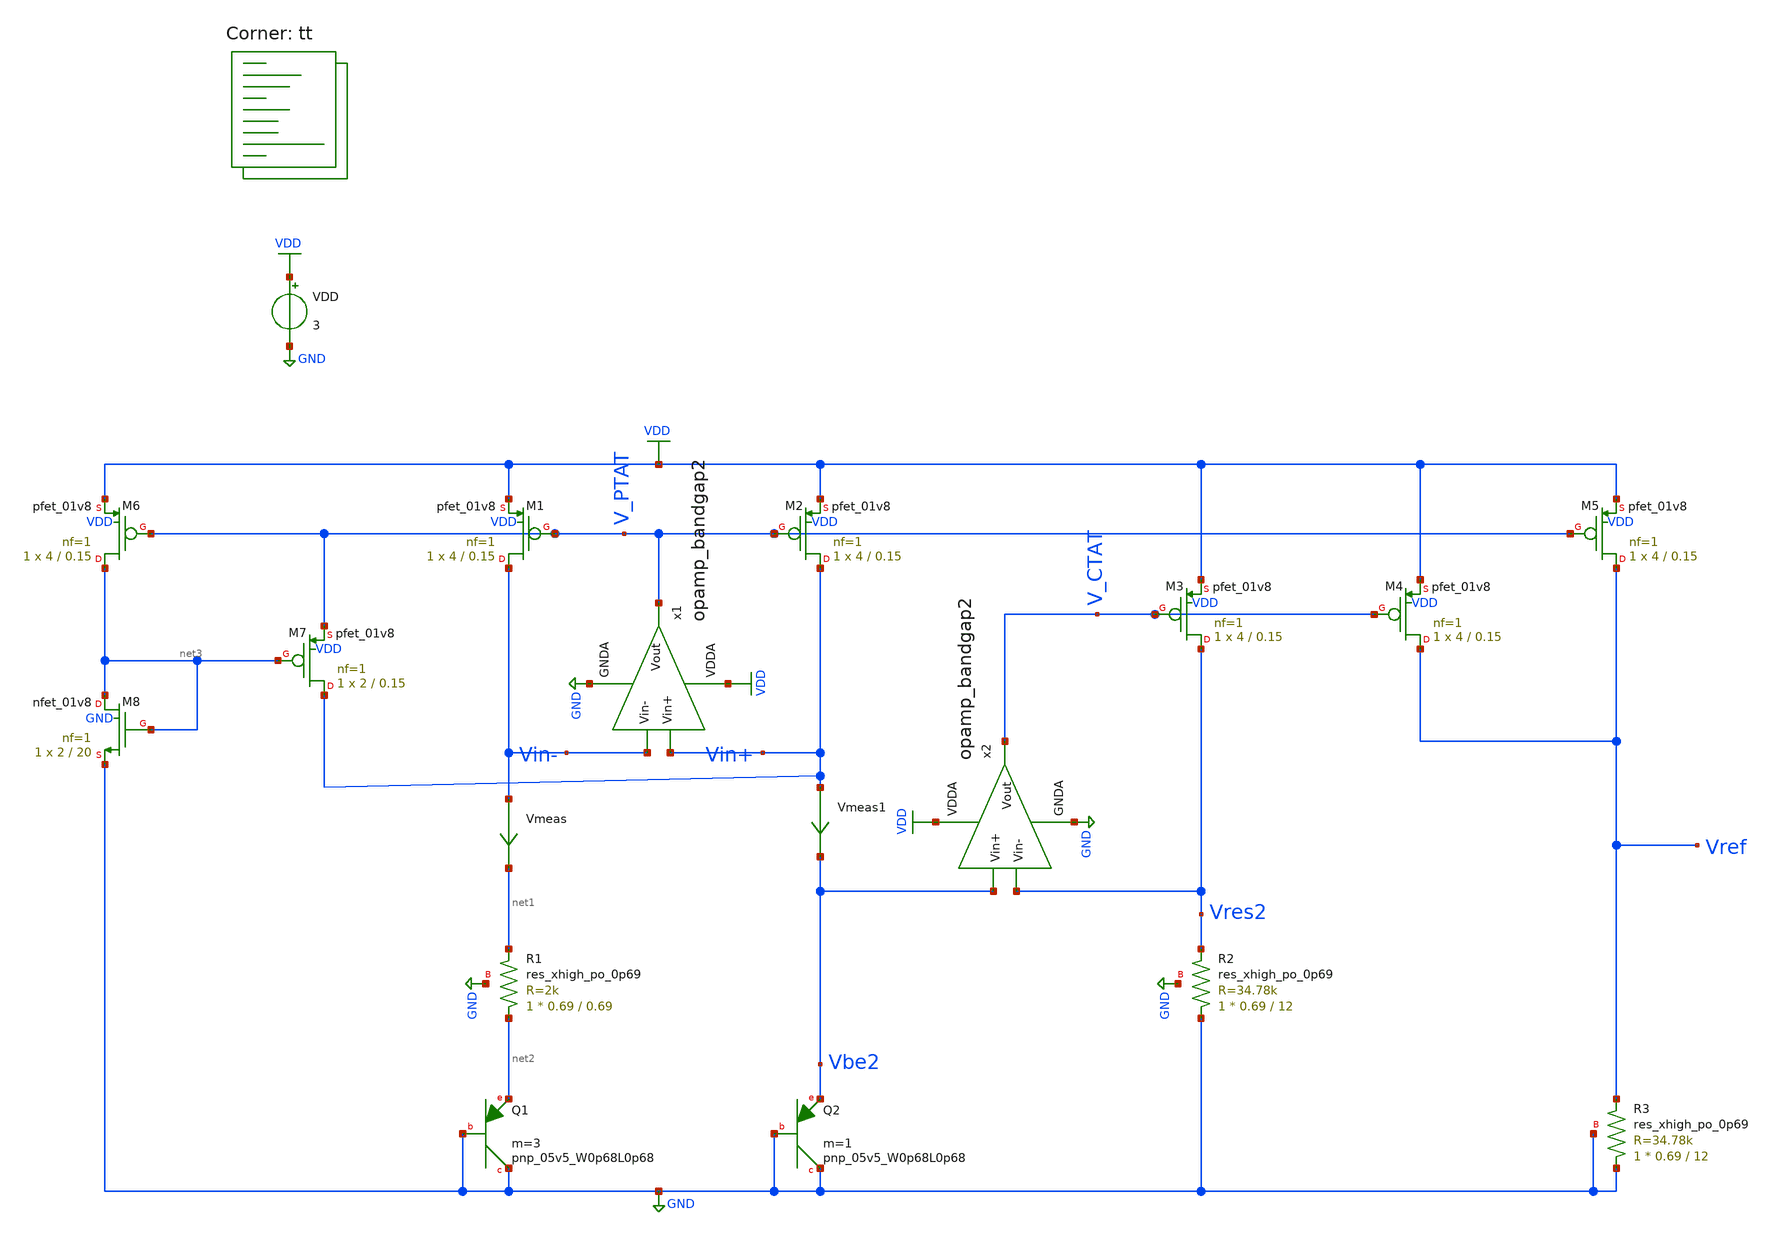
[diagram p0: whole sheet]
** sch_path: projects/bandgapref/xschem_ngspice/old_files/mos_bandgap_baker6.sch
**.subckt mos_bandgap_baker6
VDD VDD GND 3
Vmeas Vin- net1 0
.save i(vmeas)
Vmeas1 Vin+ Vbe2 0
.save i(vmeas1)
x1 VDD V_PTAT Vin- Vin+ GND opamp_bandgap2
XQ1 GND GND net2 sky130_fd_pr__pnp_05v5_W0p68L0p68 m=3
XQ2 GND GND Vbe2 sky130_fd_pr__pnp_05v5_W0p68L0p68 m=1
XR1 net2 net1 GND sky130_fd_pr__res_xhigh_po_0p69 L=0.69 mult=1 m=1
XM1 Vin- V_PTAT VDD VDD sky130_fd_pr__pfet_01v8 L=0.15 W=4 nf=1 ad='int((nf+1)/2) * W/nf * 0.29' as='int((nf+2)/2) * W/nf * 0.29'
+ pd='2*int((nf+1)/2) * (W/nf + 0.29)' ps='2*int((nf+2)/2) * (W/nf + 0.29)' nrd='0.29 / W' nrs='0.29 / W'
+ sa=0 sb=0 sd=0 mult=1 m=1
XM2 Vin+ V_PTAT VDD VDD sky130_fd_pr__pfet_01v8 L=0.15 W=4 nf=1 ad='int((nf+1)/2) * W/nf * 0.29' as='int((nf+2)/2) * W/nf * 0.29'
+ pd='2*int((nf+1)/2) * (W/nf + 0.29)' ps='2*int((nf+2)/2) * (W/nf + 0.29)' nrd='0.29 / W' nrs='0.29 / W'
+ sa=0 sb=0 sd=0 mult=1 m=1
x2 VDD V_CTAT Vres2 Vbe2 GND opamp_bandgap2
XR2 GND Vres2 GND sky130_fd_pr__res_xhigh_po_0p69 L=12 mult=1 m=1
XM3 Vres2 V_CTAT VDD VDD sky130_fd_pr__pfet_01v8 L=0.15 W=4 nf=1 ad='int((nf+1)/2) * W/nf * 0.29' as='int((nf+2)/2) * W/nf * 0.29'
+ pd='2*int((nf+1)/2) * (W/nf + 0.29)' ps='2*int((nf+2)/2) * (W/nf + 0.29)' nrd='0.29 / W' nrs='0.29 / W'
+ sa=0 sb=0 sd=0 mult=1 m=1
XM4 Vref V_CTAT VDD VDD sky130_fd_pr__pfet_01v8 L=0.15 W=4 nf=1 ad='int((nf+1)/2) * W/nf * 0.29' as='int((nf+2)/2) * W/nf * 0.29'
+ pd='2*int((nf+1)/2) * (W/nf + 0.29)' ps='2*int((nf+2)/2) * (W/nf + 0.29)' nrd='0.29 / W' nrs='0.29 / W'
+ sa=0 sb=0 sd=0 mult=1 m=1
XM5 Vref V_PTAT VDD VDD sky130_fd_pr__pfet_01v8 L=0.15 W=4 nf=1 ad='int((nf+1)/2) * W/nf * 0.29' as='int((nf+2)/2) * W/nf * 0.29'
+ pd='2*int((nf+1)/2) * (W/nf + 0.29)' ps='2*int((nf+2)/2) * (W/nf + 0.29)' nrd='0.29 / W' nrs='0.29 / W'
+ sa=0 sb=0 sd=0 mult=1 m=1
XR3 GND Vref GND sky130_fd_pr__res_xhigh_po_0p69 L=12 mult=1 m=1
XM6 net3 V_PTAT VDD VDD sky130_fd_pr__pfet_01v8 L=0.15 W=4 nf=1 ad='int((nf+1)/2) * W/nf * 0.29' as='int((nf+2)/2) * W/nf * 0.29'
+ pd='2*int((nf+1)/2) * (W/nf + 0.29)' ps='2*int((nf+2)/2) * (W/nf + 0.29)' nrd='0.29 / W' nrs='0.29 / W'
+ sa=0 sb=0 sd=0 mult=1 m=1
XM7 Vin+ net3 V_PTAT VDD sky130_fd_pr__pfet_01v8 L=0.15 W=2 nf=1 ad='int((nf+1)/2) * W/nf * 0.29' as='int((nf+2)/2) * W/nf * 0.29'
+ pd='2*int((nf+1)/2) * (W/nf + 0.29)' ps='2*int((nf+2)/2) * (W/nf + 0.29)' nrd='0.29 / W' nrs='0.29 / W'
+ sa=0 sb=0 sd=0 mult=1 m=1
XM8 net3 net3 GND GND sky130_fd_pr__nfet_01v8 L=20 W=2 nf=1 ad='int((nf+1)/2) * W/nf * 0.29' as='int((nf+2)/2) * W/nf * 0.29'
+ pd='2*int((nf+1)/2) * (W/nf + 0.29)' ps='2*int((nf+2)/2) * (W/nf + 0.29)' nrd='0.29 / W' nrs='0.29 / W'
+ sa=0 sb=0 sd=0 mult=1 m=1
**** begin user architecture code
.lib $::SKYWATER_MODELS/sky130.lib.spice tt



.option method=gear
.option wnflag=1
.option savecurrents

.save @m.xm1.msky130_fd_pr__pfet_01v8[gm] @m.xm2.msky130_fd_pr__pfet_01v8[gm] @m.xm3.msky130_fd_pr__pfet_01v8[gm] @m.xm4.msky130_fd_pr__pfet_01v8[gm] @m.xm5.msky130_fd_pr__pfet_01v8[gm] @m.xm6.msky130_fd_pr__pfet_01v8[gm] @m.xm7.msky130_fd_pr__pfet_01v8[gm] @m.xm8.msky130_fd_pr__nfet_01v8[gm]

.control
  save all
  op
  dc VDD 0 3.3 0.1 temp -40 120 1
  * tran 4ns 40us
  remzerovec
  write mos_bandgap_baker6.raw
  set appendwrite
.endc




**** end user architecture code
**.ends

* expanding   symbol:
*+  /foss/designs/my_design/projects/pll/bandgapref/xschem_ngspice/opamp_bandgap2.sym # of pins=5
** sym_path: projects/bandgapref/xschem_ngspice/old_files/opamp_bandgap2.sym
** sch_path: projects/bandgapref/xschem_ngspice/old_files/opamp_bandgap2.sch
.subckt opamp_bandgap2 VDDA Vout Vin- Vin+ GNDA
*.ipin Vin+
*.opin Vout
*.ipin Vin-
*.ipin GNDA
*.ipin VDDA
XM2 net2 Vin- net1 GNDA sky130_fd_pr__nfet_01v8 L=0.6 W=2 nf=2 ad='int((nf+1)/2) * W/nf * 0.29' as='int((nf+2)/2) * W/nf * 0.29'
+ pd='2*int((nf+1)/2) * (W/nf + 0.29)' ps='2*int((nf+2)/2) * (W/nf + 0.29)' nrd='0.29 / W' nrs='0.29 / W'
+ sa=0 sb=0 sd=0 mult=1 m=1
XM3 Vout Vin+ net1 GNDA sky130_fd_pr__nfet_01v8 L=0.6 W=2 nf=2 ad='int((nf+1)/2) * W/nf * 0.29' as='int((nf+2)/2) * W/nf * 0.29'
+ pd='2*int((nf+1)/2) * (W/nf + 0.29)' ps='2*int((nf+2)/2) * (W/nf + 0.29)' nrd='0.29 / W' nrs='0.29 / W'
+ sa=0 sb=0 sd=0 mult=1 m=1
XM1 net1 net1 GNDA GNDA sky130_fd_pr__nfet_01v8 L=0.6 W=4 nf=1 ad='int((nf+1)/2) * W/nf * 0.29' as='int((nf+2)/2) * W/nf * 0.29'
+ pd='2*int((nf+1)/2) * (W/nf + 0.29)' ps='2*int((nf+2)/2) * (W/nf + 0.29)' nrd='0.29 / W' nrs='0.29 / W'
+ sa=0 sb=0 sd=0 mult=1 m=1
XM4 Vout net2 VDDA VDDA sky130_fd_pr__pfet_01v8 L=0.6 W=4 nf=4 ad='int((nf+1)/2) * W/nf * 0.29' as='int((nf+2)/2) * W/nf * 0.29'
+ pd='2*int((nf+1)/2) * (W/nf + 0.29)' ps='2*int((nf+2)/2) * (W/nf + 0.29)' nrd='0.29 / W' nrs='0.29 / W'
+ sa=0 sb=0 sd=0 mult=1 m=1
XM5 net2 net2 VDDA VDDA sky130_fd_pr__pfet_01v8 L=0.6 W=4 nf=4 ad='int((nf+1)/2) * W/nf * 0.29' as='int((nf+2)/2) * W/nf * 0.29'
+ pd='2*int((nf+1)/2) * (W/nf + 0.29)' ps='2*int((nf+2)/2) * (W/nf + 0.29)' nrd='0.29 / W' nrs='0.29 / W'
+ sa=0 sb=0 sd=0 mult=1 m=1
.ends

.GLOBAL GND
.GLOBAL VDD
.end
